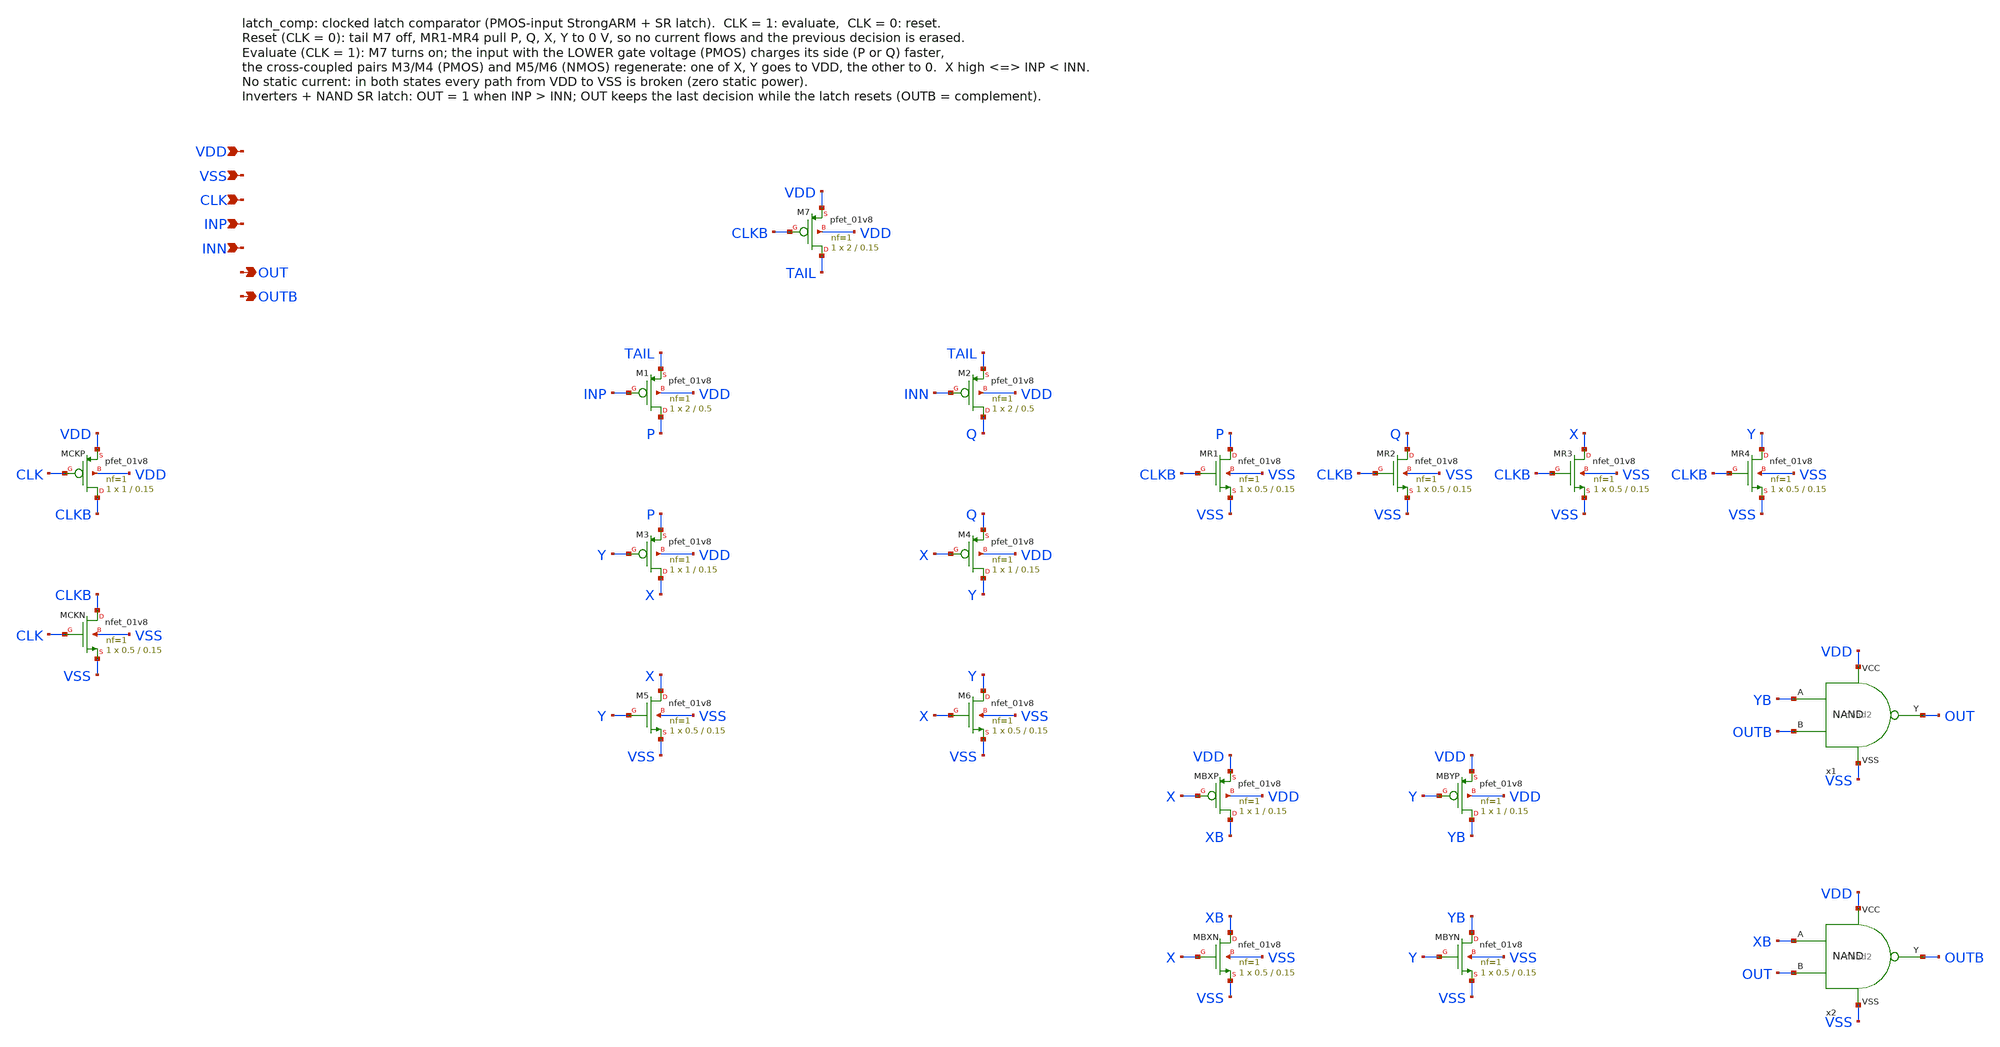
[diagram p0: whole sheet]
** sch_path: latch_comp.sch
**.subckt latch_comp VDD VSS CLK INP INN OUT OUTB
*.ipin VDD
*.ipin VSS
*.ipin CLK
*.ipin INP
*.ipin INN
*.opin OUT
*.opin OUTB
XMCKP CLKB CLK VDD VDD sky130_fd_pr__pfet_01v8 L=0.15 W=1 nf=1 ad='int((nf+1)/2) * W/nf * 0.29' as='int((nf+2)/2) * W/nf * 0.29'
+ pd='2*int((nf+1)/2) * (W/nf + 0.29)' ps='2*int((nf+2)/2) * (W/nf + 0.29)' nrd='0.29 / W' nrs='0.29 / W'
+ sa=0 sb=0 sd=0 mult=1 m=1
XMCKN CLKB CLK VSS VSS sky130_fd_pr__nfet_01v8 L=0.15 W=0.5 nf=1 ad='int((nf+1)/2) * W/nf * 0.29' as='int((nf+2)/2) * W/nf * 0.29'
+ pd='2*int((nf+1)/2) * (W/nf + 0.29)' ps='2*int((nf+2)/2) * (W/nf + 0.29)' nrd='0.29 / W' nrs='0.29 / W'
+ sa=0 sb=0 sd=0 mult=1 m=1
XM7 TAIL CLKB VDD VDD sky130_fd_pr__pfet_01v8 L=0.15 W=2 nf=1 ad='int((nf+1)/2) * W/nf * 0.29' as='int((nf+2)/2) * W/nf * 0.29'
+ pd='2*int((nf+1)/2) * (W/nf + 0.29)' ps='2*int((nf+2)/2) * (W/nf + 0.29)' nrd='0.29 / W' nrs='0.29 / W'
+ sa=0 sb=0 sd=0 mult=1 m=1
XM1 P INP TAIL VDD sky130_fd_pr__pfet_01v8 L=0.5 W=2 nf=1 ad='int((nf+1)/2) * W/nf * 0.29' as='int((nf+2)/2) * W/nf * 0.29'
+ pd='2*int((nf+1)/2) * (W/nf + 0.29)' ps='2*int((nf+2)/2) * (W/nf + 0.29)' nrd='0.29 / W' nrs='0.29 / W'
+ sa=0 sb=0 sd=0 mult=1 m=1
XM2 Q INN TAIL VDD sky130_fd_pr__pfet_01v8 L=0.5 W=2 nf=1 ad='int((nf+1)/2) * W/nf * 0.29' as='int((nf+2)/2) * W/nf * 0.29'
+ pd='2*int((nf+1)/2) * (W/nf + 0.29)' ps='2*int((nf+2)/2) * (W/nf + 0.29)' nrd='0.29 / W' nrs='0.29 / W'
+ sa=0 sb=0 sd=0 mult=1 m=1
XM3 X Y P VDD sky130_fd_pr__pfet_01v8 L=0.15 W=1 nf=1 ad='int((nf+1)/2) * W/nf * 0.29' as='int((nf+2)/2) * W/nf * 0.29'
+ pd='2*int((nf+1)/2) * (W/nf + 0.29)' ps='2*int((nf+2)/2) * (W/nf + 0.29)' nrd='0.29 / W' nrs='0.29 / W'
+ sa=0 sb=0 sd=0 mult=1 m=1
XM4 Y X Q VDD sky130_fd_pr__pfet_01v8 L=0.15 W=1 nf=1 ad='int((nf+1)/2) * W/nf * 0.29' as='int((nf+2)/2) * W/nf * 0.29'
+ pd='2*int((nf+1)/2) * (W/nf + 0.29)' ps='2*int((nf+2)/2) * (W/nf + 0.29)' nrd='0.29 / W' nrs='0.29 / W'
+ sa=0 sb=0 sd=0 mult=1 m=1
XM5 X Y VSS VSS sky130_fd_pr__nfet_01v8 L=0.15 W=0.5 nf=1 ad='int((nf+1)/2) * W/nf * 0.29' as='int((nf+2)/2) * W/nf * 0.29'
+ pd='2*int((nf+1)/2) * (W/nf + 0.29)' ps='2*int((nf+2)/2) * (W/nf + 0.29)' nrd='0.29 / W' nrs='0.29 / W'
+ sa=0 sb=0 sd=0 mult=1 m=1
XM6 Y X VSS VSS sky130_fd_pr__nfet_01v8 L=0.15 W=0.5 nf=1 ad='int((nf+1)/2) * W/nf * 0.29' as='int((nf+2)/2) * W/nf * 0.29'
+ pd='2*int((nf+1)/2) * (W/nf + 0.29)' ps='2*int((nf+2)/2) * (W/nf + 0.29)' nrd='0.29 / W' nrs='0.29 / W'
+ sa=0 sb=0 sd=0 mult=1 m=1
XMR1 P CLKB VSS VSS sky130_fd_pr__nfet_01v8 L=0.15 W=0.5 nf=1 ad='int((nf+1)/2) * W/nf * 0.29' as='int((nf+2)/2) * W/nf * 0.29'
+ pd='2*int((nf+1)/2) * (W/nf + 0.29)' ps='2*int((nf+2)/2) * (W/nf + 0.29)' nrd='0.29 / W' nrs='0.29 / W'
+ sa=0 sb=0 sd=0 mult=1 m=1
XMR2 Q CLKB VSS VSS sky130_fd_pr__nfet_01v8 L=0.15 W=0.5 nf=1 ad='int((nf+1)/2) * W/nf * 0.29' as='int((nf+2)/2) * W/nf * 0.29'
+ pd='2*int((nf+1)/2) * (W/nf + 0.29)' ps='2*int((nf+2)/2) * (W/nf + 0.29)' nrd='0.29 / W' nrs='0.29 / W'
+ sa=0 sb=0 sd=0 mult=1 m=1
XMR3 X CLKB VSS VSS sky130_fd_pr__nfet_01v8 L=0.15 W=0.5 nf=1 ad='int((nf+1)/2) * W/nf * 0.29' as='int((nf+2)/2) * W/nf * 0.29'
+ pd='2*int((nf+1)/2) * (W/nf + 0.29)' ps='2*int((nf+2)/2) * (W/nf + 0.29)' nrd='0.29 / W' nrs='0.29 / W'
+ sa=0 sb=0 sd=0 mult=1 m=1
XMR4 Y CLKB VSS VSS sky130_fd_pr__nfet_01v8 L=0.15 W=0.5 nf=1 ad='int((nf+1)/2) * W/nf * 0.29' as='int((nf+2)/2) * W/nf * 0.29'
+ pd='2*int((nf+1)/2) * (W/nf + 0.29)' ps='2*int((nf+2)/2) * (W/nf + 0.29)' nrd='0.29 / W' nrs='0.29 / W'
+ sa=0 sb=0 sd=0 mult=1 m=1
XMBXP XB X VDD VDD sky130_fd_pr__pfet_01v8 L=0.15 W=1 nf=1 ad='int((nf+1)/2) * W/nf * 0.29' as='int((nf+2)/2) * W/nf * 0.29'
+ pd='2*int((nf+1)/2) * (W/nf + 0.29)' ps='2*int((nf+2)/2) * (W/nf + 0.29)' nrd='0.29 / W' nrs='0.29 / W'
+ sa=0 sb=0 sd=0 mult=1 m=1
XMBXN XB X VSS VSS sky130_fd_pr__nfet_01v8 L=0.15 W=0.5 nf=1 ad='int((nf+1)/2) * W/nf * 0.29' as='int((nf+2)/2) * W/nf * 0.29'
+ pd='2*int((nf+1)/2) * (W/nf + 0.29)' ps='2*int((nf+2)/2) * (W/nf + 0.29)' nrd='0.29 / W' nrs='0.29 / W'
+ sa=0 sb=0 sd=0 mult=1 m=1
XMBYP YB Y VDD VDD sky130_fd_pr__pfet_01v8 L=0.15 W=1 nf=1 ad='int((nf+1)/2) * W/nf * 0.29' as='int((nf+2)/2) * W/nf * 0.29'
+ pd='2*int((nf+1)/2) * (W/nf + 0.29)' ps='2*int((nf+2)/2) * (W/nf + 0.29)' nrd='0.29 / W' nrs='0.29 / W'
+ sa=0 sb=0 sd=0 mult=1 m=1
XMBYN YB Y VSS VSS sky130_fd_pr__nfet_01v8 L=0.15 W=0.5 nf=1 ad='int((nf+1)/2) * W/nf * 0.29' as='int((nf+2)/2) * W/nf * 0.29'
+ pd='2*int((nf+1)/2) * (W/nf + 0.29)' ps='2*int((nf+2)/2) * (W/nf + 0.29)' nrd='0.29 / W' nrs='0.29 / W'
+ sa=0 sb=0 sd=0 mult=1 m=1
x1 YB OUTB OUT VDD VSS nand2
x2 XB OUT OUTB VDD VSS nand2
**.ends

* expanding   symbol:  /home/ttuser/Documents/ADCAnalogDesign/nand2.sym # of pins=5
** sym_path: nand2.sym
** sch_path: nand2.sch
.subckt nand2 A B Y VCC VSS
*.ipin A
*.ipin B
*.opin Y
*.iopin VCC
*.iopin VSS
XM1 Y A VCC VCC sky130_fd_pr__pfet_01v8 L=0.15 W=2 nf=1 ad='int((nf+1)/2) * W/nf * 0.29' as='int((nf+2)/2) * W/nf * 0.29'
+ pd='2*int((nf+1)/2) * (W/nf + 0.29)' ps='2*int((nf+2)/2) * (W/nf + 0.29)' nrd='0.29 / W' nrs='0.29 / W'
+ sa=0 sb=0 sd=0 mult=1 m=1
XM2 Y B VCC VCC sky130_fd_pr__pfet_01v8 L=0.15 W=2 nf=1 ad='int((nf+1)/2) * W/nf * 0.29' as='int((nf+2)/2) * W/nf * 0.29'
+ pd='2*int((nf+1)/2) * (W/nf + 0.29)' ps='2*int((nf+2)/2) * (W/nf + 0.29)' nrd='0.29 / W' nrs='0.29 / W'
+ sa=0 sb=0 sd=0 mult=1 m=1
XM3 Y A N1 VSS sky130_fd_pr__nfet_01v8 L=0.15 W=2 nf=1 ad='int((nf+1)/2) * W/nf * 0.29' as='int((nf+2)/2) * W/nf * 0.29'
+ pd='2*int((nf+1)/2) * (W/nf + 0.29)' ps='2*int((nf+2)/2) * (W/nf + 0.29)' nrd='0.29 / W' nrs='0.29 / W'
+ sa=0 sb=0 sd=0 mult=1 m=1
XM4 N1 B VSS VSS sky130_fd_pr__nfet_01v8 L=0.15 W=2 nf=1 ad='int((nf+1)/2) * W/nf * 0.29' as='int((nf+2)/2) * W/nf * 0.29'
+ pd='2*int((nf+1)/2) * (W/nf + 0.29)' ps='2*int((nf+2)/2) * (W/nf + 0.29)' nrd='0.29 / W' nrs='0.29 / W'
+ sa=0 sb=0 sd=0 mult=1 m=1
.ends

.end
